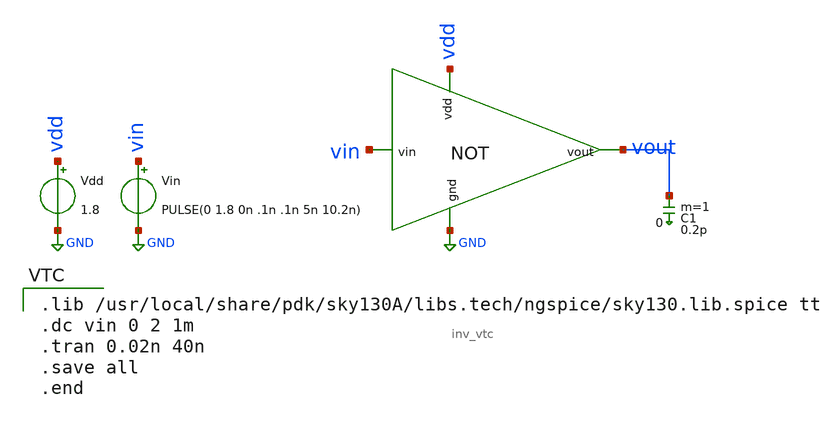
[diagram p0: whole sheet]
** sch_path: schematic/inv_test.sch
**.subckt inv_test
Vdd vdd GND 1.8
Vin vin GND PULSE(0 1.8 0n .1n .1n 5n 10.2n)
x1 vdd vout vin GND inv_vtc
C1 vout 0 0.2p m=1
**** begin user architecture code

.lib /usr/local/share/pdk/sky130A/libs.tech/ngspice/sky130.lib.spice tt
.dc vin 0 2 1m
.tran 0.02n 40n
.save all
.end

**** end user architecture code
**.ends

* expanding   symbol:  /home/subramanian/VLSI projects/CMOS/inv_vtc.sym # of pins=4
** sym_path: schematic/inv_vtc.sym
** sch_path: schematic/inv_vtc.sch
.subckt inv_vtc vdd vout vin gnd
*.ipin vin
*.ipin vdd
*.opin vout
*.ipin gnd
XM1 vout vin gnd gnd sky130_fd_pr__nfet_01v8 L=0.15 W=1 nf=1 ad='int((1 + 1)/2) * 1 / 1 * 0.29' as='int((1 + 2)/2) * 1 / 1 * 0.29'
+ pd='2*int((1 + 1)/2) * (1 / 1 + 0.29)' ps='2*int((1 + 2)/2) * (1 / 1 + 0.29)' nrd='0.29 / 1 ' nrs='0.29 / 1 '
+ sa=0 sb=0 sd=0 mult=1 m=1
XM2 vout vin vdd vdd sky130_fd_pr__pfet_01v8 L=0.15 W=2 nf=1 ad='int((1 + 1)/2) * 2 / 1 * 0.29' as='int((1 + 2)/2) * 2 / 1 * 0.29'
+ pd='2*int((1 + 1)/2) * (2 / 1 + 0.29)' ps='2*int((1 + 2)/2) * (2 / 1 + 0.29)' nrd='0.29 / 2 ' nrs='0.29 / 2 '
+ sa=0 sb=0 sd=0 mult=1 m=1
.ends

.GLOBAL GND
.end
